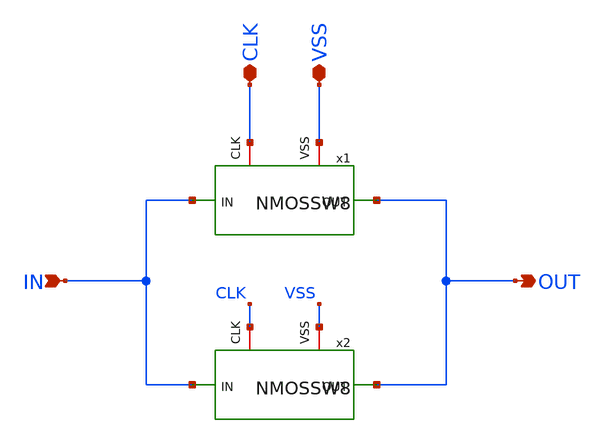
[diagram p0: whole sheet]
** sch_path: NMOSSW16.sch
**.subckt NMOSSW16 IN OUT VSS CLK
*.ipin IN
*.opin OUT
*.iopin VSS
*.iopin CLK
x1 CLK VSS OUT IN NMOSSW8
x2 CLK VSS OUT IN NMOSSW8
**.ends

* expanding   symbol:  NMOSSW8.sym # of pins=4
** sym_path: NMOSSW8.sym
** sch_path: NMOSSW8.sch
.subckt NMOSSW8 CLK VSS OUT IN
*.ipin IN
*.opin OUT
*.iopin VSS
*.iopin CLK
x1 CLK VSS OUT IN NMOSSW4
x2 CLK VSS OUT IN NMOSSW4
.ends


* expanding   symbol:  NMOSSW4.sym # of pins=4
** sym_path: NMOSSW4.sym
** sch_path: NMOSSW4.sch
.subckt NMOSSW4 CLK VSS OUT IN
*.ipin IN
*.opin OUT
*.iopin VSS
*.iopin CLK
x1 CLK VSS OUT IN NMOSSW2
x2 CLK VSS OUT IN NMOSSW2
.ends


* expanding   symbol:  NMOSSW2.sym # of pins=4
** sym_path: NMOSSW2.sym
** sch_path: NMOSSW2.sch
.subckt NMOSSW2 CLK VSS OUT IN
*.ipin IN
*.opin OUT
*.iopin VSS
*.iopin CLK
x1 CLK VSS OUT IN NMOSSW
x2 CLK VSS OUT IN NMOSSW
.ends


* expanding   symbol:  NMOSSW.sym # of pins=4
** sym_path: NMOSSW.sym
** sch_path: NMOSSW.sch
.subckt NMOSSW CLK VSS OUT IN
*.ipin IN
*.iopin VSS
*.opin OUT
*.iopin CLK
M1 OUT CLK IN VSS nch w=10u l=0.35u as=0 ps=0 ad=0 pd=0 m=1
.ends

.end
